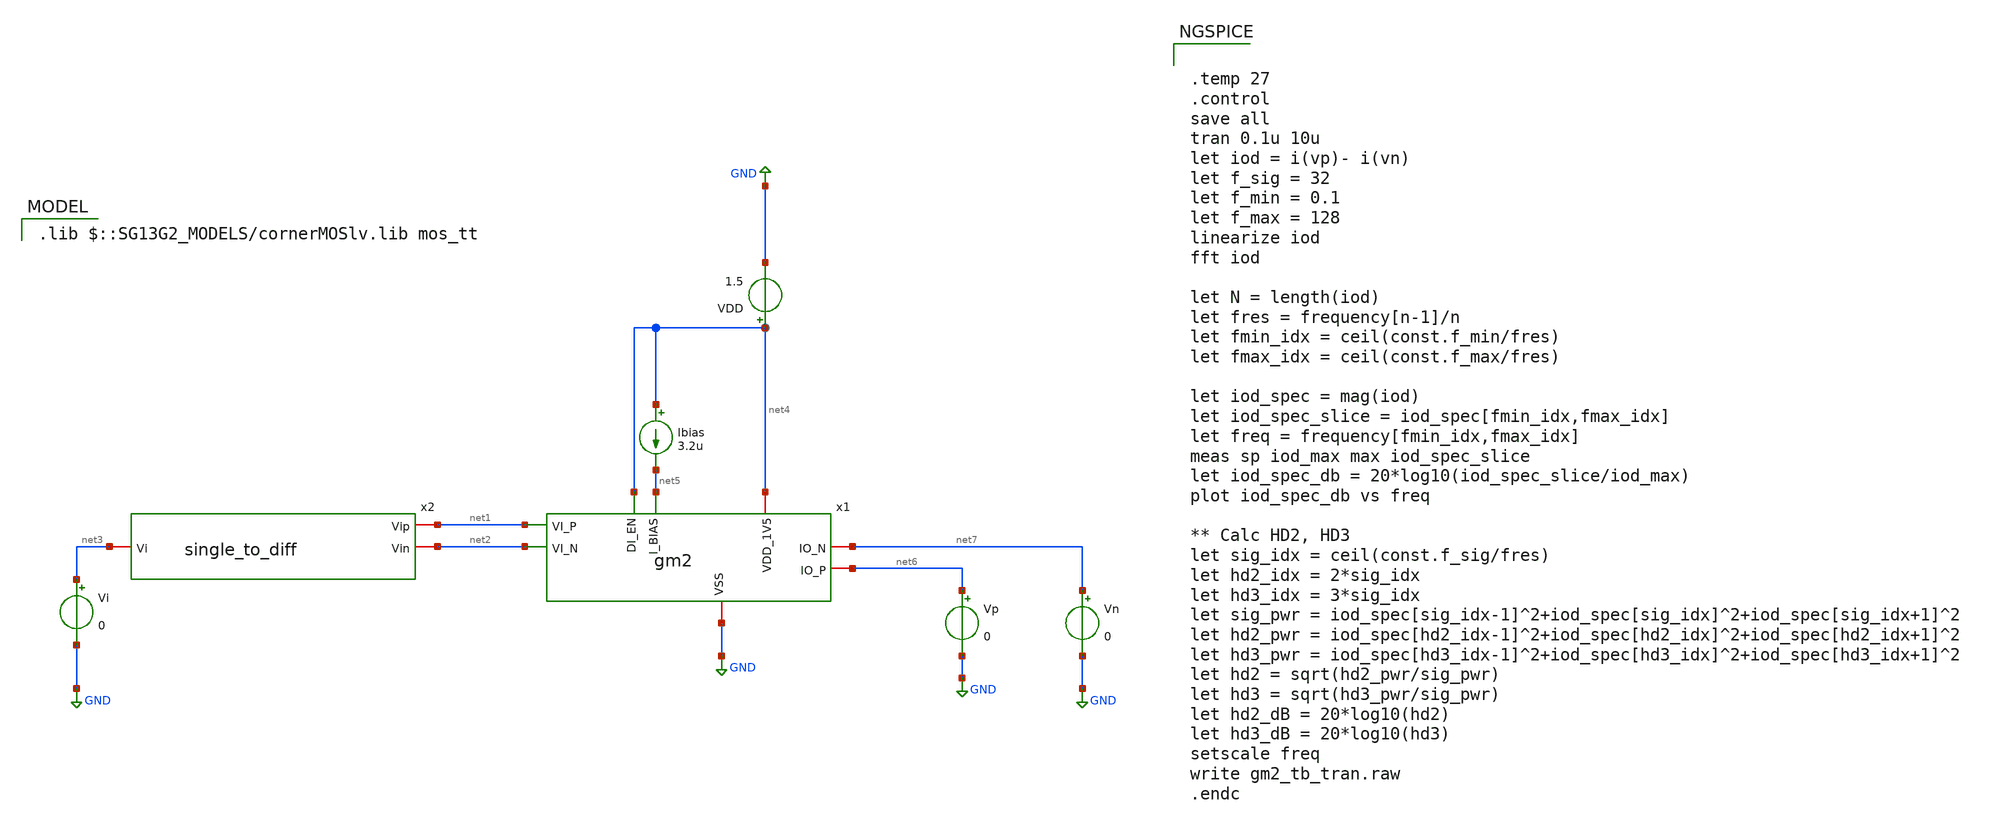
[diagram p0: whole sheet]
** sch_path: gm2_tb_tran.sch
**.subckt gm2_tb_tran
x1 net4 net5 net7 net6 net2 net1 net4 GND gm2
x2 net1 net2 net3 single_to_diff
Vi net3 GND 0
VDD net4 GND 1.5
Ibias net4 net5 3.2u
Vp net6 GND 0
Vn net7 GND 0
**** begin user architecture code


.save @n.x1.xm1.nsg13_lv_nmos[gm]
.save @n.x1.xm1.nsg13_lv_nmos[vth]
.save @n.x1.xm1.nsg13_lv_nmos[cgg]
.save @n.x1.xm1.nsg13_lv_nmos[vdss]
.save @n.x1.xm1.nsg13_lv_nmos[ids]
.save @n.x1.xm1.nsg13_lv_nmos[vds]
.save @n.x1.xm1.nsg13_lv_nmos[fug]
.save @n.x1.xm1.nsg13_lv_nmos[vgs]


.save @n.x1.xm2.nsg13_lv_nmos[gm]
.save @n.x1.xm2.nsg13_lv_nmos[vth]
.save @n.x1.xm2.nsg13_lv_nmos[cgg]
.save @n.x1.xm2.nsg13_lv_nmos[vdss]
.save @n.x1.xm2.nsg13_lv_nmos[ids]
.save @n.x1.xm2.nsg13_lv_nmos[vds]
.save @n.x1.xm2.nsg13_lv_nmos[fug]
.save @n.x1.xm2.nsg13_lv_nmos[vgs]


.save @n.x1.xm3.nsg13_lv_pmos[gm]
.save @n.x1.xm3.nsg13_lv_pmos[vth]
.save @n.x1.xm3.nsg13_lv_pmos[cgg]
.save @n.x1.xm3.nsg13_lv_pmos[vdss]
.save @n.x1.xm3.nsg13_lv_pmos[ids]
.save @n.x1.xm3.nsg13_lv_pmos[vds]
.save @n.x1.xm3.nsg13_lv_pmos[fug]
.save @n.x1.xm3.nsg13_lv_pmos[vgs]


.save @n.x1.xm4.nsg13_lv_pmos[gm]
.save @n.x1.xm4.nsg13_lv_pmos[vth]
.save @n.x1.xm4.nsg13_lv_pmos[cgg]
.save @n.x1.xm4.nsg13_lv_pmos[vdss]
.save @n.x1.xm4.nsg13_lv_pmos[ids]
.save @n.x1.xm4.nsg13_lv_pmos[vds]
.save @n.x1.xm4.nsg13_lv_pmos[fug]
.save @n.x1.xm4.nsg13_lv_pmos[vgs]


.save @n.x1.xm5.nsg13_lv_nmos[gm]
.save @n.x1.xm5.nsg13_lv_nmos[vth]
.save @n.x1.xm5.nsg13_lv_nmos[cgg]
.save @n.x1.xm5.nsg13_lv_nmos[vdss]
.save @n.x1.xm5.nsg13_lv_nmos[ids]
.save @n.x1.xm5.nsg13_lv_nmos[vds]
.save @n.x1.xm5.nsg13_lv_nmos[fug]
.save @n.x1.xm5.nsg13_lv_nmos[vgs]


.save @n.x1.xm6.nsg13_lv_nmos[gm]
.save @n.x1.xm6.nsg13_lv_nmos[vth]
.save @n.x1.xm6.nsg13_lv_nmos[cgg]
.save @n.x1.xm6.nsg13_lv_nmos[vdss]
.save @n.x1.xm6.nsg13_lv_nmos[ids]
.save @n.x1.xm6.nsg13_lv_nmos[vds]
.save @n.x1.xm6.nsg13_lv_nmos[fug]
.save @n.x1.xm6.nsg13_lv_nmos[vgs]


.save @n.x1.xm7.nsg13_lv_nmos[gm]
.save @n.x1.xm7.nsg13_lv_nmos[vth]
.save @n.x1.xm7.nsg13_lv_nmos[cgg]
.save @n.x1.xm7.nsg13_lv_nmos[vdss]
.save @n.x1.xm7.nsg13_lv_nmos[ids]
.save @n.x1.xm7.nsg13_lv_nmos[vds]
.save @n.x1.xm7.nsg13_lv_nmos[fug]
.save @n.x1.xm7.nsg13_lv_nmos[vgs]


.save @n.x1.xm8.nsg13_lv_pmos[gm]
.save @n.x1.xm8.nsg13_lv_pmos[vth]
.save @n.x1.xm8.nsg13_lv_pmos[cgg]
.save @n.x1.xm8.nsg13_lv_pmos[vdss]
.save @n.x1.xm8.nsg13_lv_pmos[ids]
.save @n.x1.xm8.nsg13_lv_pmos[vds]
.save @n.x1.xm8.nsg13_lv_pmos[fug]
.save @n.x1.xm8.nsg13_lv_pmos[vgs]


.save @n.x1.xm9.nsg13_lv_nmos[gm]
.save @n.x1.xm9.nsg13_lv_nmos[vth]
.save @n.x1.xm9.nsg13_lv_nmos[cgg]
.save @n.x1.xm9.nsg13_lv_nmos[vdss]
.save @n.x1.xm9.nsg13_lv_nmos[ids]
.save @n.x1.xm9.nsg13_lv_nmos[vds]
.save @n.x1.xm9.nsg13_lv_nmos[fug]
.save @n.x1.xm9.nsg13_lv_nmos[vgs]


.save @n.x1.xm10.nsg13_lv_pmos[gm]
.save @n.x1.xm10.nsg13_lv_pmos[vth]
.save @n.x1.xm10.nsg13_lv_pmos[cgg]
.save @n.x1.xm10.nsg13_lv_pmos[vdss]
.save @n.x1.xm10.nsg13_lv_pmos[ids]
.save @n.x1.xm10.nsg13_lv_pmos[vds]
.save @n.x1.xm10.nsg13_lv_pmos[fug]
.save @n.x1.xm10.nsg13_lv_pmos[vgs]


.save @n.x1.xm11.nsg13_lv_nmos[gm]
.save @n.x1.xm11.nsg13_lv_nmos[vth]
.save @n.x1.xm11.nsg13_lv_nmos[cgg]
.save @n.x1.xm11.nsg13_lv_nmos[vdss]
.save @n.x1.xm11.nsg13_lv_nmos[ids]
.save @n.x1.xm11.nsg13_lv_nmos[vds]
.save @n.x1.xm11.nsg13_lv_nmos[fug]
.save @n.x1.xm11.nsg13_lv_nmos[vgs]


.save @n.x1.xm12.nsg13_lv_nmos[gm]
.save @n.x1.xm12.nsg13_lv_nmos[vth]
.save @n.x1.xm12.nsg13_lv_nmos[cgg]
.save @n.x1.xm12.nsg13_lv_nmos[vdss]
.save @n.x1.xm12.nsg13_lv_nmos[ids]
.save @n.x1.xm12.nsg13_lv_nmos[vds]
.save @n.x1.xm12.nsg13_lv_nmos[fug]
.save @n.x1.xm12.nsg13_lv_nmos[vgs]


.save @n.x1.xm13.nsg13_lv_nmos[gm]
.save @n.x1.xm13.nsg13_lv_nmos[vth]
.save @n.x1.xm13.nsg13_lv_nmos[cgg]
.save @n.x1.xm13.nsg13_lv_nmos[vdss]
.save @n.x1.xm13.nsg13_lv_nmos[ids]
.save @n.x1.xm13.nsg13_lv_nmos[vds]
.save @n.x1.xm13.nsg13_lv_nmos[fug]
.save @n.x1.xm13.nsg13_lv_nmos[vgs]


.save @n.x1.xm14.nsg13_lv_pmos[gm]
.save @n.x1.xm14.nsg13_lv_pmos[vth]
.save @n.x1.xm14.nsg13_lv_pmos[cgg]
.save @n.x1.xm14.nsg13_lv_pmos[vdss]
.save @n.x1.xm14.nsg13_lv_pmos[ids]
.save @n.x1.xm14.nsg13_lv_pmos[vds]
.save @n.x1.xm14.nsg13_lv_pmos[fug]
.save @n.x1.xm14.nsg13_lv_pmos[vgs]


.save @n.x1.xm15.nsg13_lv_pmos[gm]
.save @n.x1.xm15.nsg13_lv_pmos[vth]
.save @n.x1.xm15.nsg13_lv_pmos[cgg]
.save @n.x1.xm15.nsg13_lv_pmos[vdss]
.save @n.x1.xm15.nsg13_lv_pmos[ids]
.save @n.x1.xm15.nsg13_lv_pmos[vds]
.save @n.x1.xm15.nsg13_lv_pmos[fug]
.save @n.x1.xm15.nsg13_lv_pmos[vgs]


.save @n.x1.xm16.nsg13_lv_pmos[gm]
.save @n.x1.xm16.nsg13_lv_pmos[vth]
.save @n.x1.xm16.nsg13_lv_pmos[cgg]
.save @n.x1.xm16.nsg13_lv_pmos[vdss]
.save @n.x1.xm16.nsg13_lv_pmos[ids]
.save @n.x1.xm16.nsg13_lv_pmos[vds]
.save @n.x1.xm16.nsg13_lv_pmos[fug]
.save @n.x1.xm16.nsg13_lv_pmos[vgs]


.save @n.x1.xm17.nsg13_lv_pmos[gm]
.save @n.x1.xm17.nsg13_lv_pmos[vth]
.save @n.x1.xm17.nsg13_lv_pmos[cgg]
.save @n.x1.xm17.nsg13_lv_pmos[vdss]
.save @n.x1.xm17.nsg13_lv_pmos[ids]
.save @n.x1.xm17.nsg13_lv_pmos[vds]
.save @n.x1.xm17.nsg13_lv_pmos[fug]
.save @n.x1.xm17.nsg13_lv_pmos[vgs]


.save @n.x1.xm18.nsg13_lv_nmos[gm]
.save @n.x1.xm18.nsg13_lv_nmos[vth]
.save @n.x1.xm18.nsg13_lv_nmos[cgg]
.save @n.x1.xm18.nsg13_lv_nmos[vdss]
.save @n.x1.xm18.nsg13_lv_nmos[ids]
.save @n.x1.xm18.nsg13_lv_nmos[vds]
.save @n.x1.xm18.nsg13_lv_nmos[fug]
.save @n.x1.xm18.nsg13_lv_nmos[vgs]


.save @n.x1.xm19.nsg13_lv_nmos[gm]
.save @n.x1.xm19.nsg13_lv_nmos[vth]
.save @n.x1.xm19.nsg13_lv_nmos[cgg]
.save @n.x1.xm19.nsg13_lv_nmos[vdss]
.save @n.x1.xm19.nsg13_lv_nmos[ids]
.save @n.x1.xm19.nsg13_lv_nmos[vds]
.save @n.x1.xm19.nsg13_lv_nmos[fug]
.save @n.x1.xm19.nsg13_lv_nmos[vgs]


.save @n.x1.xm20.nsg13_lv_nmos[gm]
.save @n.x1.xm20.nsg13_lv_nmos[vth]
.save @n.x1.xm20.nsg13_lv_nmos[cgg]
.save @n.x1.xm20.nsg13_lv_nmos[vdss]
.save @n.x1.xm20.nsg13_lv_nmos[ids]
.save @n.x1.xm20.nsg13_lv_nmos[vds]
.save @n.x1.xm20.nsg13_lv_nmos[fug]
.save @n.x1.xm20.nsg13_lv_nmos[vgs]


.save @n.x1.xm21.nsg13_lv_nmos[gm]
.save @n.x1.xm21.nsg13_lv_nmos[vth]
.save @n.x1.xm21.nsg13_lv_nmos[cgg]
.save @n.x1.xm21.nsg13_lv_nmos[vdss]
.save @n.x1.xm21.nsg13_lv_nmos[ids]
.save @n.x1.xm21.nsg13_lv_nmos[vds]
.save @n.x1.xm21.nsg13_lv_nmos[fug]
.save @n.x1.xm21.nsg13_lv_nmos[vgs]




.temp 27
.control
save all
tran 0.1u 10u
let iod = i(vp)- i(vn)
let f_sig = 32
let f_min = 0.1
let f_max = 128
linearize iod
fft iod

let N = length(iod)
let fres = frequency[n-1]/n
let fmin_idx = ceil(const.f_min/fres)
let fmax_idx = ceil(const.f_max/fres)

let iod_spec = mag(iod)
let iod_spec_slice = iod_spec[fmin_idx,fmax_idx]
let freq = frequency[fmin_idx,fmax_idx]
meas sp iod_max max iod_spec_slice
let iod_spec_db = 20*log10(iod_spec_slice/iod_max)
plot iod_spec_db vs freq

** Calc HD2, HD3
let sig_idx = ceil(const.f_sig/fres)
let hd2_idx = 2*sig_idx
let hd3_idx = 3*sig_idx
let sig_pwr = iod_spec[sig_idx-1]^2+iod_spec[sig_idx]^2+iod_spec[sig_idx+1]^2
let hd2_pwr = iod_spec[hd2_idx-1]^2+iod_spec[hd2_idx]^2+iod_spec[hd2_idx+1]^2
let hd3_pwr = iod_spec[hd3_idx-1]^2+iod_spec[hd3_idx]^2+iod_spec[hd3_idx+1]^2
let hd2 = sqrt(hd2_pwr/sig_pwr)
let hd3 = sqrt(hd3_pwr/sig_pwr)
let hd2_dB = 20*log10(hd2)
let hd3_dB = 20*log10(hd3)
setscale freq
write gm2_tb_tran.raw
.endc


 .lib $::SG13G2_MODELS/cornerMOSlv.lib mos_tt

**** end user architecture code
**.ends

* expanding   symbol:  gm2.sym # of pins=8
** sym_path: gm2.sym
** sch_path: gm2.sch
.subckt gm2 VDD_1V5 I_BIAS IO_N IO_P VI_N VI_P DI_EN VSS
*.ipin VI_N
*.ipin VI_P
*.iopin VSS
*.iopin VDD_1V5
*.iopin IO_P
*.iopin IO_N
*.ipin I_BIAS
*.ipin DI_EN
XM1 I_drain1 VI_P Vsp Vsp sg13_lv_nmos w=1u l=1u ng=1 m=1 mm_ok=1
XM2 I_drain2 VI_N Vsn Vsn sg13_lv_nmos w=1u l=1u ng=1 m=1 mm_ok=1
Rs Vsp Vsn 500k m=1
XM5 Vsp V_dg VSS VSS sg13_lv_nmos w=0.5u l=1u ng=1 m=1 mm_ok=1
XM6 Vsn V_dg VSS VSS sg13_lv_nmos w=0.5u l=1u ng=1 m=1 mm_ok=1
XM7 V_dg V_dg VSS VSS sg13_lv_nmos w=1u l=1u ng=1 m=1 mm_ok=1
XM8 net1 DI_EN VDD_1V5 VDD_1V5 sg13_lv_pmos w=1u l=0.13u ng=1 m=1 mm_ok=1
XM9 enable net1 VSS VSS sg13_lv_nmos w=1u l=0.13u ng=1 m=1 mm_ok=1
XM10 enable net1 VDD_1V5 VDD_1V5 sg13_lv_pmos w=1u l=0.13u ng=1 m=1 mm_ok=1
XM11 net1 DI_EN VSS VSS sg13_lv_nmos w=1u l=0.13u ng=1 m=1 mm_ok=1
XM12 I_BIAS enable V_dg VSS sg13_lv_nmos w=1u l=0.13u ng=1 m=1 mm_ok=1
XM3 I_drain1 I_drain1 VDD_1V5 VDD_1V5 sg13_lv_pmos w=1u l=1u ng=1 m=1 mm_ok=1
XM4 I_drain2 I_drain2 VDD_1V5 VDD_1V5 sg13_lv_pmos w=1u l=1u ng=1 m=1 mm_ok=1
XM14 Vds_1 I_drain1 VDD_1V5 VDD_1V5 sg13_lv_pmos w=1u l=1u ng=1 m=1 mm_ok=1
XM15 Vds_2 I_drain2 VDD_1V5 VDD_1V5 sg13_lv_pmos w=1u l=1u ng=1 m=1 mm_ok=1
XM13 V_dg net1 VSS VSS sg13_lv_nmos w=1u l=1u ng=1 m=1 mm_ok=1
XM16 IO_P I_drain1 VDD_1V5 VDD_1V5 sg13_lv_pmos w=2u l=1u ng=1 m=1 mm_ok=1
XM17 IO_N I_drain2 VDD_1V5 VDD_1V5 sg13_lv_pmos w=2u l=1u ng=1 m=1 mm_ok=1
XM18 IO_P Vds_1 VSS VSS sg13_lv_nmos w=0.74u l=1u ng=1 m=1 mm_ok=1
XM19 Vds_1 Vds_1 VSS VSS sg13_lv_nmos w=1u l=1u ng=1 m=1 mm_ok=1
XM20 Vds_2 Vds_2 VSS VSS sg13_lv_nmos w=1u l=1u ng=1 m=1 mm_ok=1
XM21 IO_N Vds_2 VSS VSS sg13_lv_nmos w=0.74u l=1u ng=1 m=1 mm_ok=1
.ends


* expanding   symbol:  single_to_diff.sym # of pins=3
** sym_path: single_to_diff.sym
** sch_path: single_to_diff.sch
.subckt single_to_diff Vip Vin Vi
*.iopin Vi
*.iopin Vip
*.iopin Vin
E1 net1 GND Vi GND 1
E2 Vin net2 net1 GND -0.5
E3 Vip net2 net1 GND 0.5
Vcm net2 GND 0.75
.ends

.GLOBAL GND
.end
